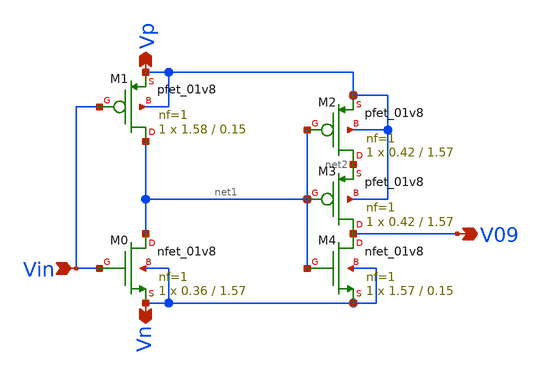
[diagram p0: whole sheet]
** sch_path: xschem/Vth_sch/Symbol/th09.sch
**.subckt th09 Vin V09 Vn Vp
*.ipin Vin
*.opin V09
*.opin Vn
*.opin Vp
XM2 net2 net1 Vp Vp sky130_fd_pr__pfet_01v8 L=1.57 W=0.42 nf=1 ad='int((nf+1)/2) * W/nf * 0.29' as='int((nf+2)/2) * W/nf * 0.29'
+ pd='2*int((nf+1)/2) * (W/nf + 0.29)' ps='2*int((nf+2)/2) * (W/nf + 0.29)' nrd='0.29 / W' nrs='0.29 / W'
+ sa=0 sb=0 sd=0 mult=1 m=1
XM3 V09 net1 net2 Vp sky130_fd_pr__pfet_01v8 L=1.57 W=0.42 nf=1 ad='int((nf+1)/2) * W/nf * 0.29' as='int((nf+2)/2) * W/nf * 0.29'
+ pd='2*int((nf+1)/2) * (W/nf + 0.29)' ps='2*int((nf+2)/2) * (W/nf + 0.29)' nrd='0.29 / W' nrs='0.29 / W'
+ sa=0 sb=0 sd=0 mult=1 m=1
XM4 V09 net1 Vn Vn sky130_fd_pr__nfet_01v8 L=0.15 W=1.57 nf=1 ad='int((nf+1)/2) * W/nf * 0.29' as='int((nf+2)/2) * W/nf * 0.29'
+ pd='2*int((nf+1)/2) * (W/nf + 0.29)' ps='2*int((nf+2)/2) * (W/nf + 0.29)' nrd='0.29 / W' nrs='0.29 / W'
+ sa=0 sb=0 sd=0 mult=1 m=1
XM1 net1 Vin Vp Vp sky130_fd_pr__pfet_01v8 L=0.15 W=1.58 nf=1 ad='int((nf+1)/2) * W/nf * 0.29' as='int((nf+2)/2) * W/nf * 0.29'
+ pd='2*int((nf+1)/2) * (W/nf + 0.29)' ps='2*int((nf+2)/2) * (W/nf + 0.29)' nrd='0.29 / W' nrs='0.29 / W'
+ sa=0 sb=0 sd=0 mult=1 m=1
XM0 net1 Vin Vn Vn sky130_fd_pr__nfet_01v8 L=1.57 W=0.36 nf=1 ad='int((nf+1)/2) * W/nf * 0.29' as='int((nf+2)/2) * W/nf * 0.29'
+ pd='2*int((nf+1)/2) * (W/nf + 0.29)' ps='2*int((nf+2)/2) * (W/nf + 0.29)' nrd='0.29 / W' nrs='0.29 / W'
+ sa=0 sb=0 sd=0 mult=1 m=1
**.ends
.end
